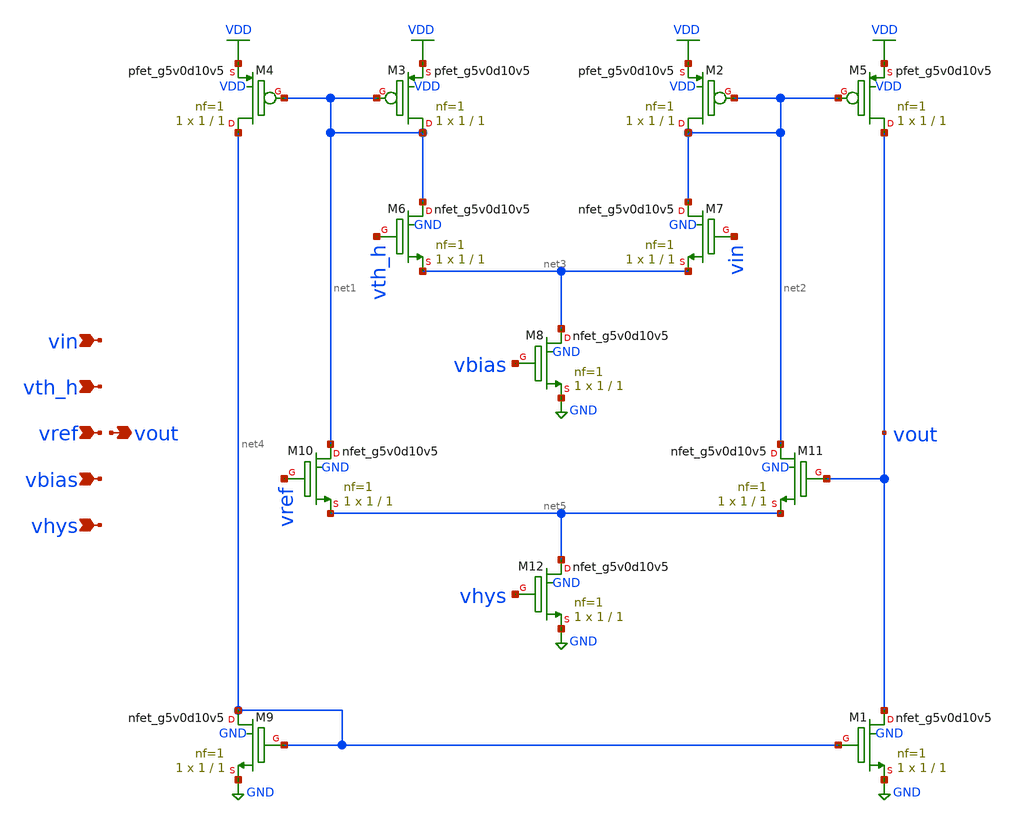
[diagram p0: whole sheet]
** sch_path: schematics/hysteresis_comparator.sch
**.subckt hysteresis_comparator vin vout vth_h vref vbias vhys
*.ipin vin
*.opin vout
*.ipin vth_h
*.ipin vref
*.ipin vbias
*.ipin vhys
XM3 net1 net1 VDD VDD sky130_fd_pr__pfet_g5v0d10v5 L=1 W=1 nf=1 ad='int((nf+1)/2) * W/nf * 0.29' as='int((nf+2)/2) * W/nf * 0.29'
+ pd='2*int((nf+1)/2) * (W/nf + 0.29)' ps='2*int((nf+2)/2) * (W/nf + 0.29)' nrd='0.29 / W' nrs='0.29 / W'
+ sa=0 sb=0 sd=0 mult=1 m=1
XM1 vout net4 GND GND sky130_fd_pr__nfet_g5v0d10v5 L=1 W=1 nf=1 ad='int((nf+1)/2) * W/nf * 0.29' as='int((nf+2)/2) * W/nf * 0.29'
+ pd='2*int((nf+1)/2) * (W/nf + 0.29)' ps='2*int((nf+2)/2) * (W/nf + 0.29)' nrd='0.29 / W' nrs='0.29 / W'
+ sa=0 sb=0 sd=0 mult=1 m=1
XM2 net2 net2 VDD VDD sky130_fd_pr__pfet_g5v0d10v5 L=1 W=1 nf=1 ad='int((nf+1)/2) * W/nf * 0.29' as='int((nf+2)/2) * W/nf * 0.29'
+ pd='2*int((nf+1)/2) * (W/nf + 0.29)' ps='2*int((nf+2)/2) * (W/nf + 0.29)' nrd='0.29 / W' nrs='0.29 / W'
+ sa=0 sb=0 sd=0 mult=1 m=1
XM4 net4 net1 VDD VDD sky130_fd_pr__pfet_g5v0d10v5 L=1 W=1 nf=1 ad='int((nf+1)/2) * W/nf * 0.29' as='int((nf+2)/2) * W/nf * 0.29'
+ pd='2*int((nf+1)/2) * (W/nf + 0.29)' ps='2*int((nf+2)/2) * (W/nf + 0.29)' nrd='0.29 / W' nrs='0.29 / W'
+ sa=0 sb=0 sd=0 mult=1 m=1
XM5 vout net2 VDD VDD sky130_fd_pr__pfet_g5v0d10v5 L=1 W=1 nf=1 ad='int((nf+1)/2) * W/nf * 0.29' as='int((nf+2)/2) * W/nf * 0.29'
+ pd='2*int((nf+1)/2) * (W/nf + 0.29)' ps='2*int((nf+2)/2) * (W/nf + 0.29)' nrd='0.29 / W' nrs='0.29 / W'
+ sa=0 sb=0 sd=0 mult=1 m=1
XM6 net1 vth_h net3 GND sky130_fd_pr__nfet_g5v0d10v5 L=1 W=1 nf=1 ad='int((nf+1)/2) * W/nf * 0.29' as='int((nf+2)/2) * W/nf * 0.29'
+ pd='2*int((nf+1)/2) * (W/nf + 0.29)' ps='2*int((nf+2)/2) * (W/nf + 0.29)' nrd='0.29 / W' nrs='0.29 / W'
+ sa=0 sb=0 sd=0 mult=1 m=1
XM7 net2 vin net3 GND sky130_fd_pr__nfet_g5v0d10v5 L=1 W=1 nf=1 ad='int((nf+1)/2) * W/nf * 0.29' as='int((nf+2)/2) * W/nf * 0.29'
+ pd='2*int((nf+1)/2) * (W/nf + 0.29)' ps='2*int((nf+2)/2) * (W/nf + 0.29)' nrd='0.29 / W' nrs='0.29 / W'
+ sa=0 sb=0 sd=0 mult=1 m=1
XM8 net3 vbias GND GND sky130_fd_pr__nfet_g5v0d10v5 L=1 W=1 nf=1 ad='int((nf+1)/2) * W/nf * 0.29' as='int((nf+2)/2) * W/nf * 0.29'
+ pd='2*int((nf+1)/2) * (W/nf + 0.29)' ps='2*int((nf+2)/2) * (W/nf + 0.29)' nrd='0.29 / W' nrs='0.29 / W'
+ sa=0 sb=0 sd=0 mult=1 m=1
XM9 net4 net4 GND GND sky130_fd_pr__nfet_g5v0d10v5 L=1 W=1 nf=1 ad='int((nf+1)/2) * W/nf * 0.29' as='int((nf+2)/2) * W/nf * 0.29'
+ pd='2*int((nf+1)/2) * (W/nf + 0.29)' ps='2*int((nf+2)/2) * (W/nf + 0.29)' nrd='0.29 / W' nrs='0.29 / W'
+ sa=0 sb=0 sd=0 mult=1 m=1
XM10 net1 vref net5 GND sky130_fd_pr__nfet_g5v0d10v5 L=1 W=1 nf=1 ad='int((nf+1)/2) * W/nf * 0.29' as='int((nf+2)/2) * W/nf * 0.29'
+ pd='2*int((nf+1)/2) * (W/nf + 0.29)' ps='2*int((nf+2)/2) * (W/nf + 0.29)' nrd='0.29 / W' nrs='0.29 / W'
+ sa=0 sb=0 sd=0 mult=1 m=1
XM11 net2 vout net5 GND sky130_fd_pr__nfet_g5v0d10v5 L=1 W=1 nf=1 ad='int((nf+1)/2) * W/nf * 0.29' as='int((nf+2)/2) * W/nf * 0.29'
+ pd='2*int((nf+1)/2) * (W/nf + 0.29)' ps='2*int((nf+2)/2) * (W/nf + 0.29)' nrd='0.29 / W' nrs='0.29 / W'
+ sa=0 sb=0 sd=0 mult=1 m=1
XM12 net5 vhys GND GND sky130_fd_pr__nfet_g5v0d10v5 L=1 W=1 nf=1 ad='int((nf+1)/2) * W/nf * 0.29' as='int((nf+2)/2) * W/nf * 0.29'
+ pd='2*int((nf+1)/2) * (W/nf + 0.29)' ps='2*int((nf+2)/2) * (W/nf + 0.29)' nrd='0.29 / W' nrs='0.29 / W'
+ sa=0 sb=0 sd=0 mult=1 m=1
**.ends
.GLOBAL VDD
.GLOBAL GND
.end
